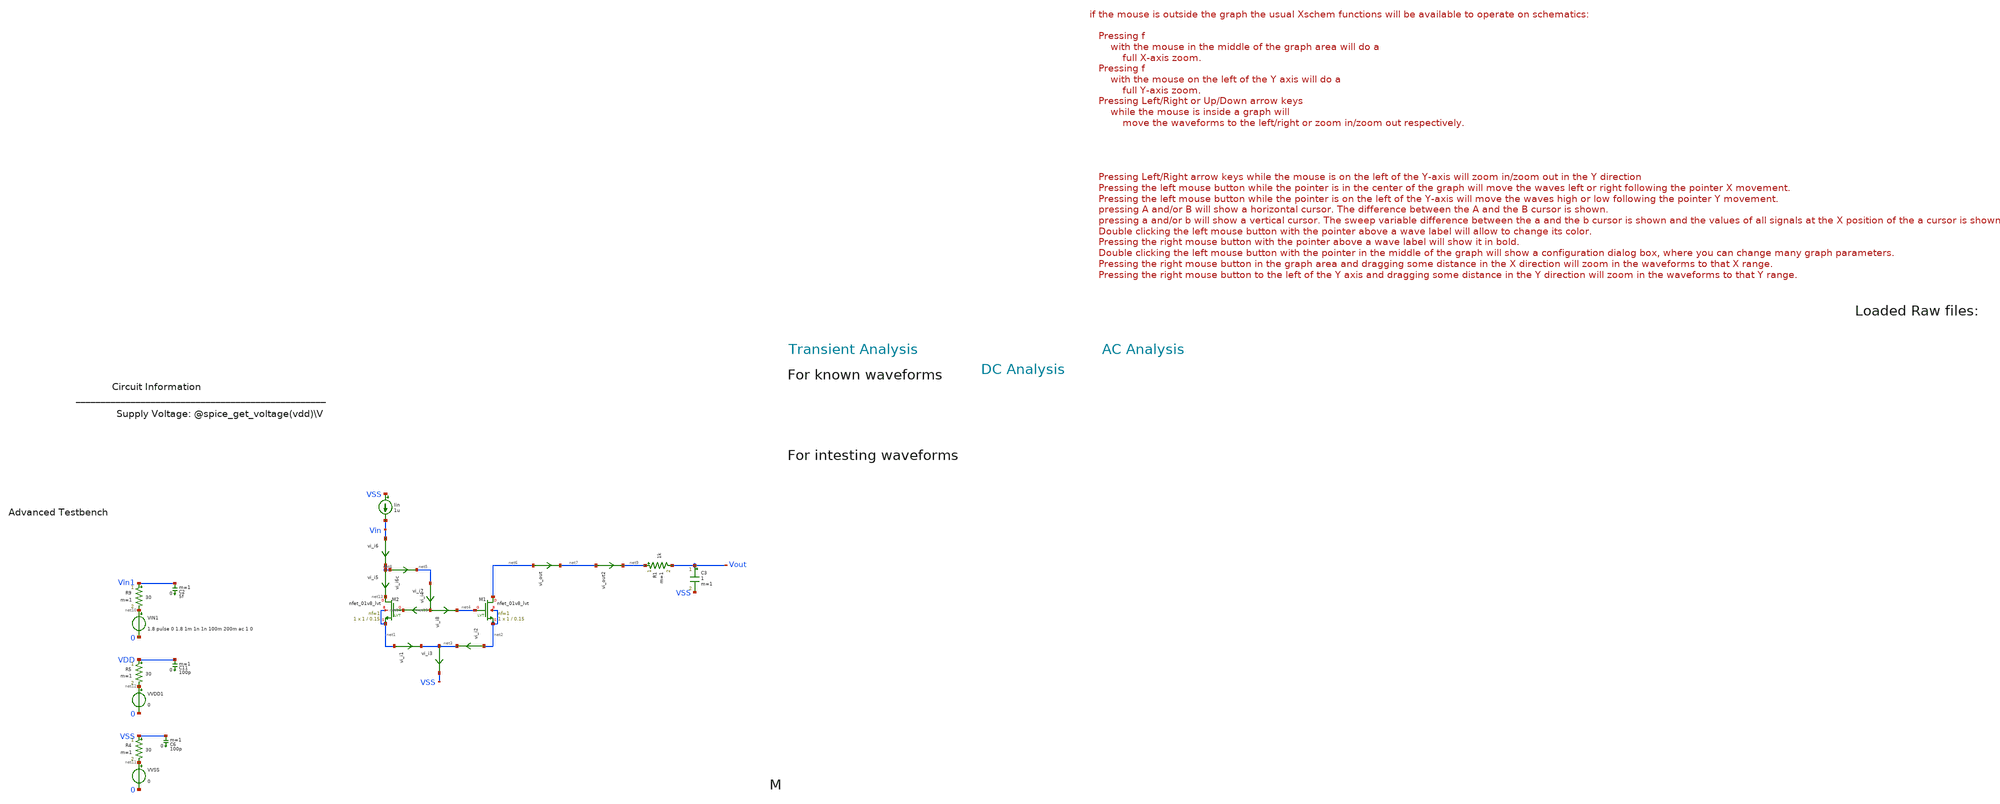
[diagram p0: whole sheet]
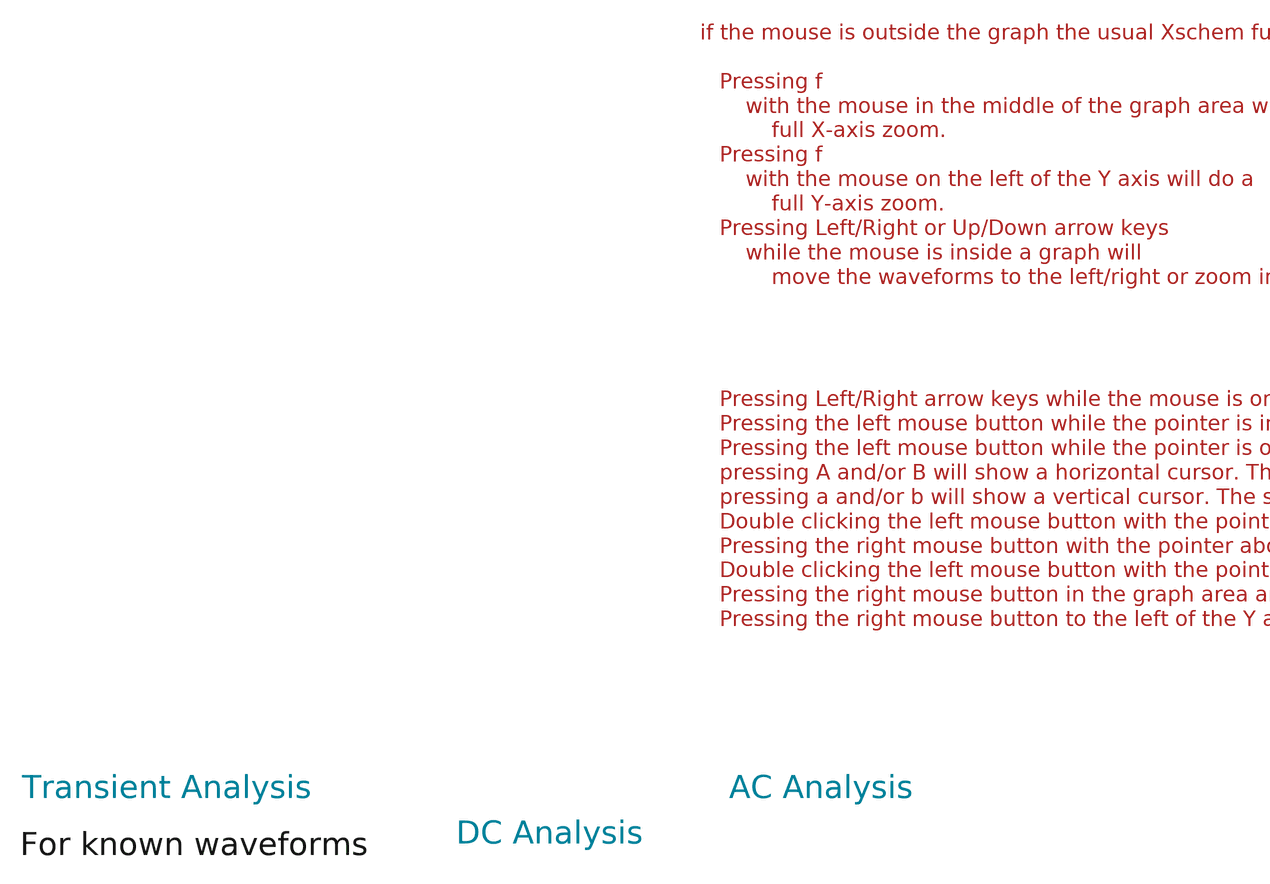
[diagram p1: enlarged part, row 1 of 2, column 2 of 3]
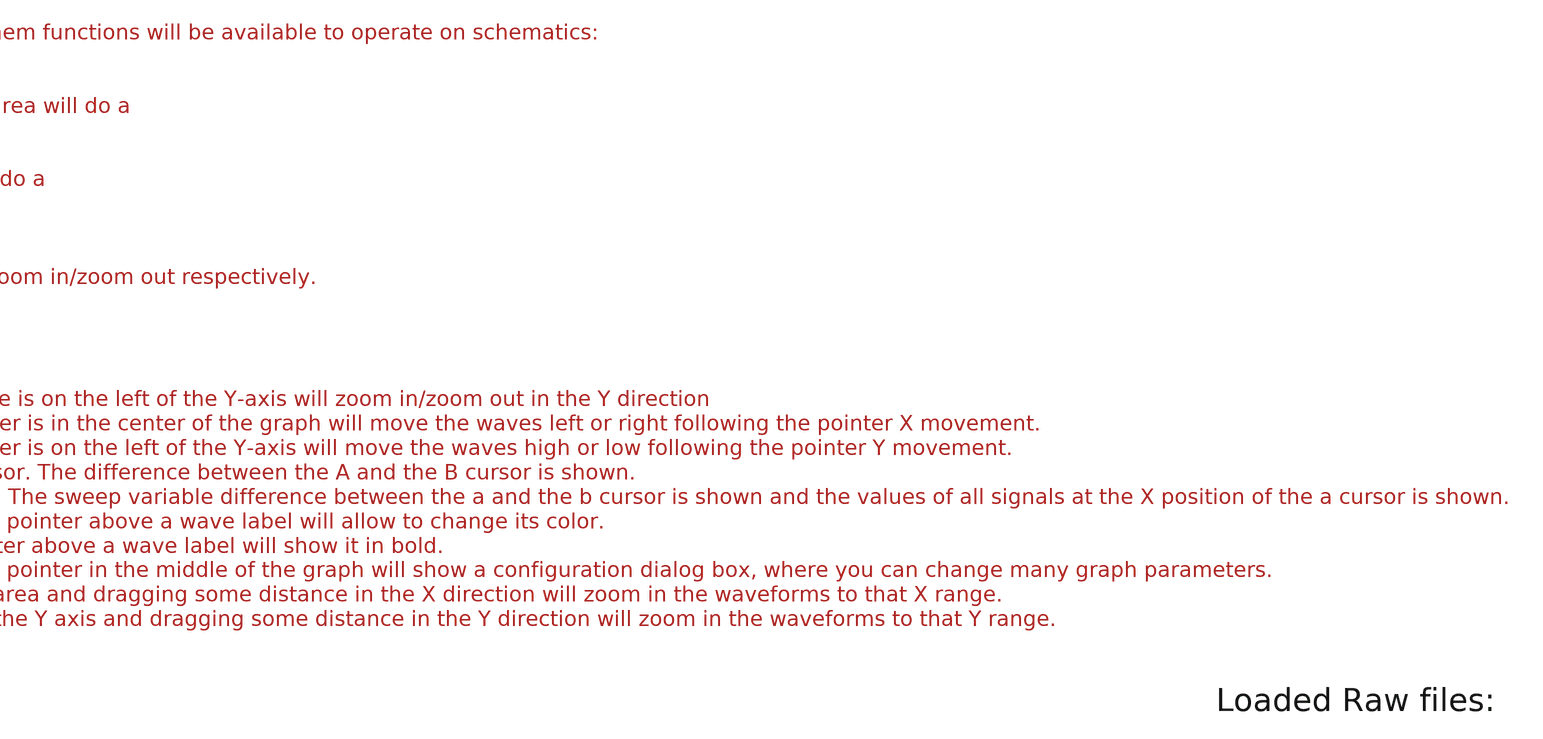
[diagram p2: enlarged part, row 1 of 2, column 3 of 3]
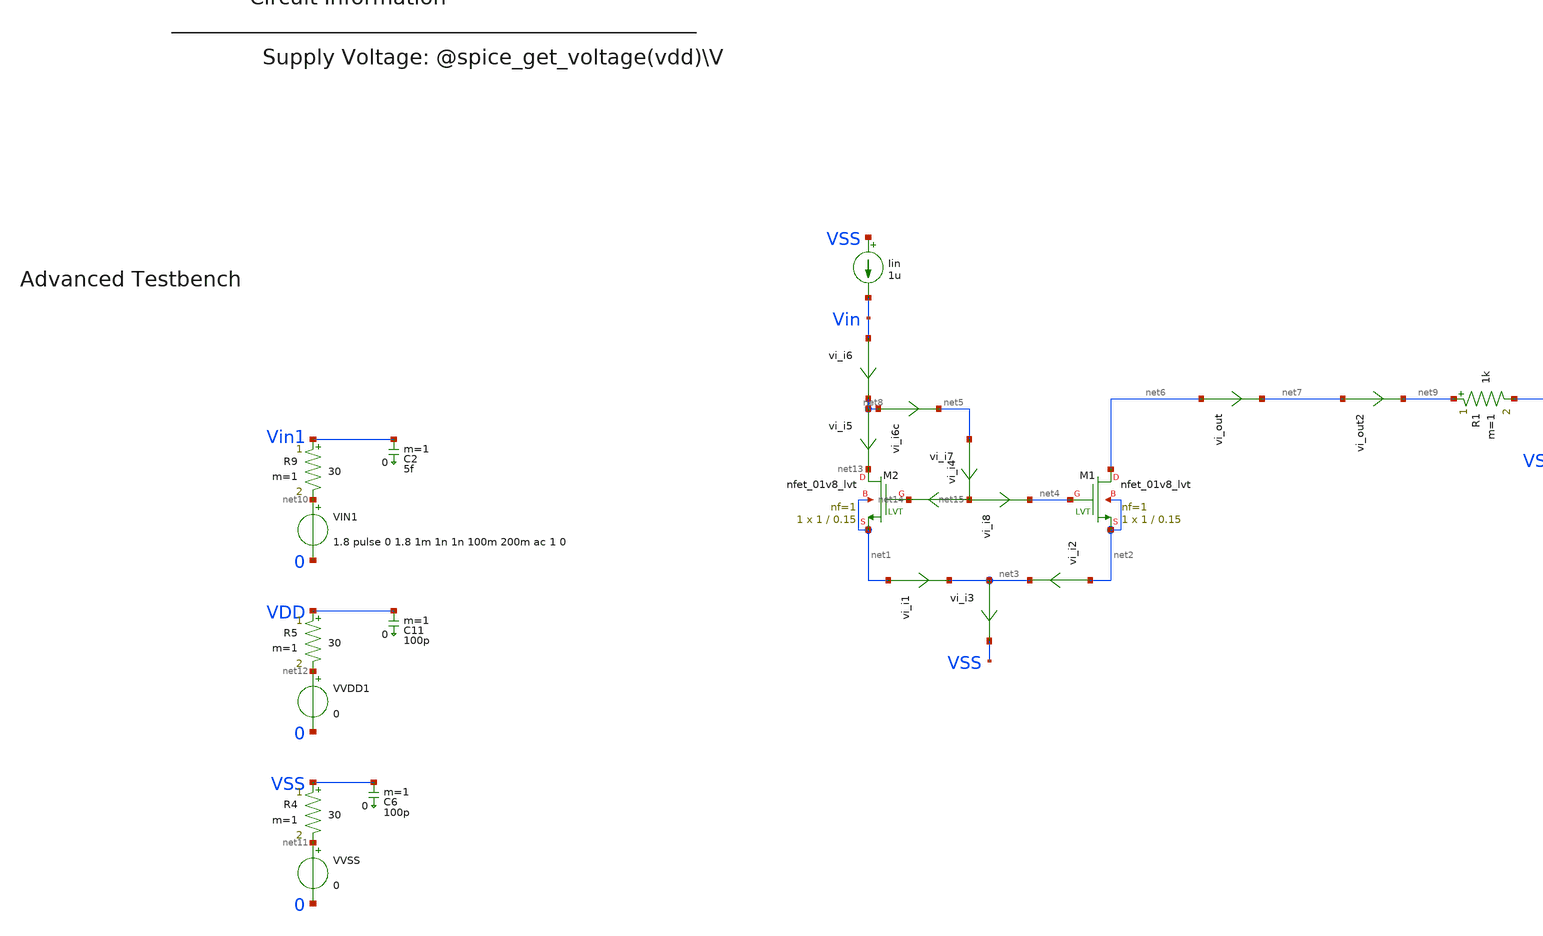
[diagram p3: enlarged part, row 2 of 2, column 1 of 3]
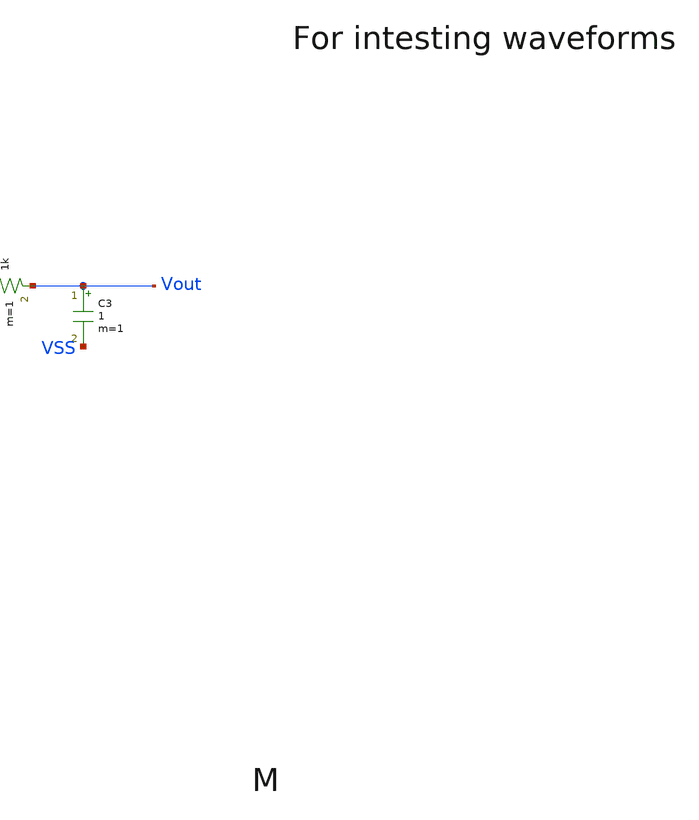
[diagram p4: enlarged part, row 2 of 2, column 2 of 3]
** sch_path: tt10-hdl/tt_um_test_commit/xschem/T0/currMirr/curr_mirror_tb.sch
* Copyright (C) 1998-2024 Stefan Frederik Schippers
* This program is free software; you can redistribute it and/or modify
* it under the terms of the GNU General Public License as published by
* the Free Software Foundation; either version 2 of the License, or
* (at your option) any later version.
* This program is distributed in the hope that it will be useful,
* but WITHOUT ANY WARRANTY; without even the implied warranty of
* MERCHANTABILITY or FITNESS FOR A PARTICULAR PURPOSE.  See the
* GNU General Public License for more details.
* You should have received a copy of the GNU General Public License
* along with this program; if not, write to the Free Software
**.subckt curr_mirror_tb
VIN1 net10 0 1.8 pulse 0 1.8 1m 1n 1n 100m 200m ac 1 0
VVSS net11 0 0
R4 VSS net11 30 m=1
C6 VSS 0 100p m=1
VVDD1 net12 0 0
R5 VDD net12 30 m=1
C11 VDD 0 100p m=1
R9 Vin1 net10 30 m=1
C2 Vin1 0 5f m=1
Iin VSS Vin 1u
XM2 net13 net14 net1 net1 sky130_fd_pr__nfet_01v8_lvt L=0.15 W=1 nf=1 ad='int((1 + 1)/2) * 1 / 1 * 0.29'
+ as='int((1 + 2)/2) * 1 / 1 * 0.29' pd='2*int((1 + 1)/2) * (1 / 1 + 0.29)' ps='2*int((1 + 2)/2) * (1 / 1 + 0.29)'
+ nrd='0.29 / 1 ' nrs='0.29 / 1 ' sa=0 sb=0 sd=0 mult=1 m=1
XM1 net6 net4 net2 net2 sky130_fd_pr__nfet_01v8_lvt L=0.15 W=1 nf=1 ad='int((1 + 1)/2) * 1 / 1 * 0.29'
+ as='int((1 + 2)/2) * 1 / 1 * 0.29' pd='2*int((1 + 1)/2) * (1 / 1 + 0.29)' ps='2*int((1 + 2)/2) * (1 / 1 + 0.29)'
+ nrd='0.29 / 1 ' nrs='0.29 / 1 ' sa=0 sb=0 sd=0 mult=1 m=1
vi_i1 net1 net3 0
.save i(vi_i1)
vi_i2 net2 net3 0
.save i(vi_i2)
vi_i3 net3 VSS 0
.save i(vi_i3)
vi_i4 net15 net14 0
.save i(vi_i4)
vi_i5 net8 net13 0
.save i(vi_i5)
vi_i6c net8 net5 0
.save i(vi_i6c)
vi_i6 Vin net8 0
.save i(vi_i6)
vi_i7 net5 net15 0
.save i(vi_i7)
vi_i8 net15 net4 0
.save i(vi_i8)
vi_out net6 net7 0
.save i(vi_out)
C3 Vout VSS 1 m=1
vi_out2 net7 net9 0
.save i(vi_out2)
R1 net9 Vout 1k m=1
**** begin user architecture code



.temp 30
*.param IB=1n
*.param VDD = 1.8

.option savecurrents
.save all @m1[gm]
.control
  save all alli
  op
  let power=-v(vdd) * i(vvdd)
  settype power power
  write template_adv_tb.raw
  set appendwrite

  *dc VDD 0 1.8 0.1
  *write template_adv_tb.raw

  tran 0.5m  500m
  write template_adv_tb.raw

  *ac dec 10 1 1G
  *remzerovec
  *write template_adv_tb.raw



  quit 0




.endc





** opencircuitdesign pdks install
.lib $::SKYWATER_MODELS/sky130.lib.spice tt
.include $::SKYWATER_STDCELLS/sky130_fd_sc_hd.spice


**** end user architecture code
**.ends
.end
